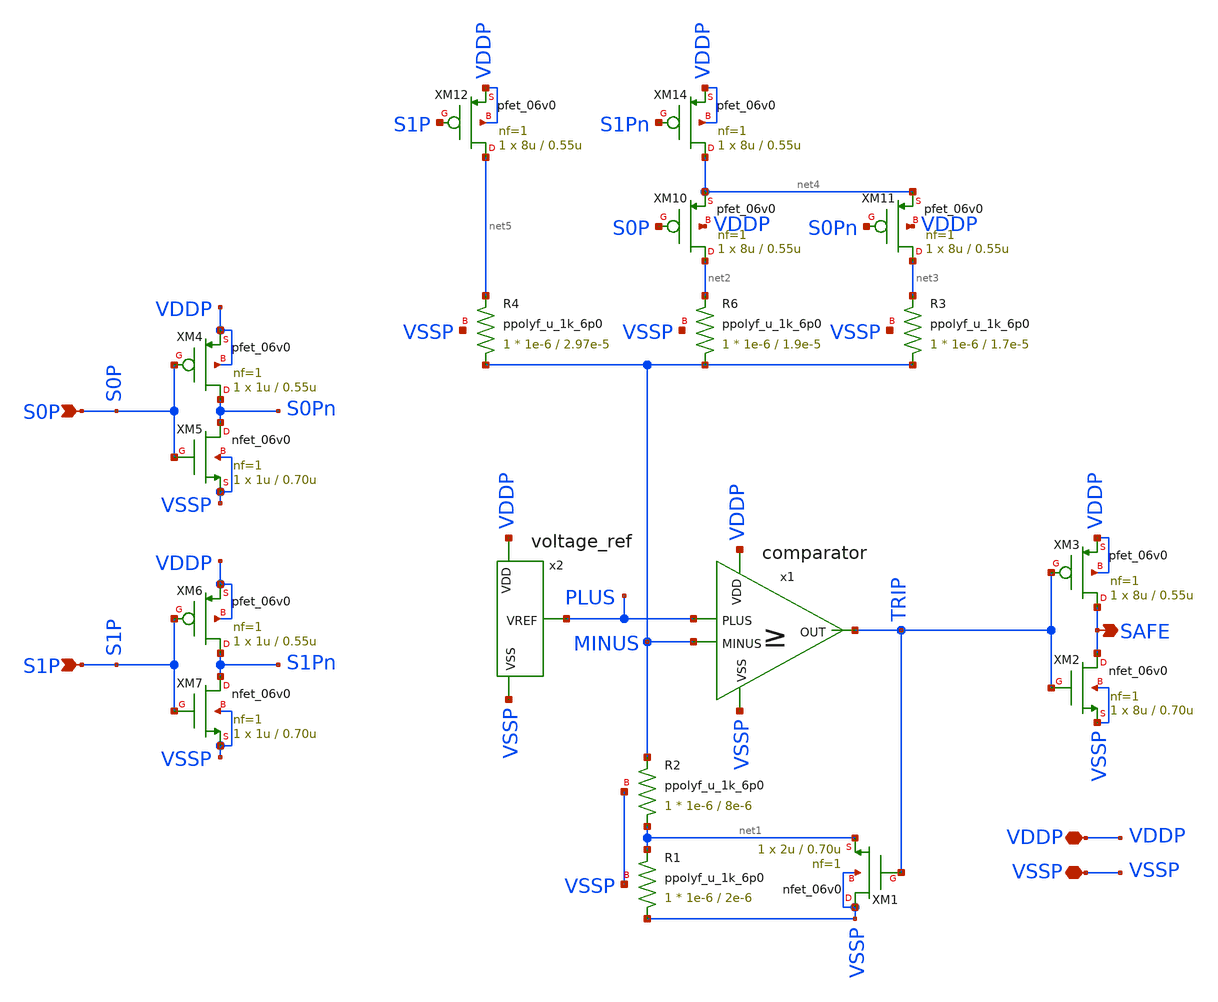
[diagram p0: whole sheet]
** sch_path: analog/xschem/overdischarge_prot.sch
**.subckt overdischarge_prot VDDP VSSP SAFE S0P S1P
*.iopin VDDP
*.iopin VSSP
*.opin SAFE
*.ipin S0P
*.ipin S1P
x1 VDDP TRIP PLUS MINUS VSSP comparator
x2 VDDP PLUS VSSP voltage_ref
XM1 VSSP TRIP net1 VSSP nfet_06v0 L=0.70u W=2u nf=1 ad='int((nf+1)/2) * W/nf * 0.18u' as='int((nf+2)/2) * W/nf * 0.18u'
+ pd='2*int((nf+1)/2) * (W/nf + 0.18u)' ps='2*int((nf+2)/2) * (W/nf + 0.18u)' nrd='0.18u / W' nrs='0.18u / W'
+ sa=0 sb=0 sd=0 m=1
XR1 VSSP net1 VSSP ppolyf_u_1k_6p0 r_width=1e-6 r_length=2e-6 m=1
XR2 net1 MINUS VSSP ppolyf_u_1k_6p0 r_width=1e-6 r_length=8e-6 m=1
XR3 MINUS net3 VSSP ppolyf_u_1k_6p0 r_width=1e-6 r_length=1.7e-5 m=1
XM2 SAFE TRIP VSSP VSSP nfet_06v0 L=0.70u W=8u nf=1 ad='int((nf+1)/2) * W/nf * 0.18u' as='int((nf+2)/2) * W/nf * 0.18u'
+ pd='2*int((nf+1)/2) * (W/nf + 0.18u)' ps='2*int((nf+2)/2) * (W/nf + 0.18u)' nrd='0.18u / W' nrs='0.18u / W'
+ sa=0 sb=0 sd=0 m=1
XM3 SAFE TRIP VDDP VDDP pfet_06v0 L=0.55u W=8u nf=1 ad='int((nf+1)/2) * W/nf * 0.18u' as='int((nf+2)/2) * W/nf * 0.18u'
+ pd='2*int((nf+1)/2) * (W/nf + 0.18u)' ps='2*int((nf+2)/2) * (W/nf + 0.18u)' nrd='0.18u / W' nrs='0.18u / W'
+ sa=0 sb=0 sd=0 m=1
XM4 S0Pn S0P VDDP VDDP pfet_06v0 L=0.55u W=1u nf=1 ad='int((nf+1)/2) * W/nf * 0.18u' as='int((nf+2)/2) * W/nf * 0.18u'
+ pd='2*int((nf+1)/2) * (W/nf + 0.18u)' ps='2*int((nf+2)/2) * (W/nf + 0.18u)' nrd='0.18u / W' nrs='0.18u / W'
+ sa=0 sb=0 sd=0 m=1
XM5 S0Pn S0P VSSP VSSP nfet_06v0 L=0.70u W=1u nf=1 ad='int((nf+1)/2) * W/nf * 0.18u' as='int((nf+2)/2) * W/nf * 0.18u'
+ pd='2*int((nf+1)/2) * (W/nf + 0.18u)' ps='2*int((nf+2)/2) * (W/nf + 0.18u)' nrd='0.18u / W' nrs='0.18u / W'
+ sa=0 sb=0 sd=0 m=1
XM6 S1Pn S1P VDDP VDDP pfet_06v0 L=0.55u W=1u nf=1 ad='int((nf+1)/2) * W/nf * 0.18u' as='int((nf+2)/2) * W/nf * 0.18u'
+ pd='2*int((nf+1)/2) * (W/nf + 0.18u)' ps='2*int((nf+2)/2) * (W/nf + 0.18u)' nrd='0.18u / W' nrs='0.18u / W'
+ sa=0 sb=0 sd=0 m=1
XM7 S1Pn S1P VSSP VSSP nfet_06v0 L=0.70u W=1u nf=1 ad='int((nf+1)/2) * W/nf * 0.18u' as='int((nf+2)/2) * W/nf * 0.18u'
+ pd='2*int((nf+1)/2) * (W/nf + 0.18u)' ps='2*int((nf+2)/2) * (W/nf + 0.18u)' nrd='0.18u / W' nrs='0.18u / W'
+ sa=0 sb=0 sd=0 m=1
XR4 MINUS net5 VSSP ppolyf_u_1k_6p0 r_width=1e-6 r_length=2.97e-5 m=1
XR6 MINUS net2 VSSP ppolyf_u_1k_6p0 r_width=1e-6 r_length=1.9e-5 m=1
XM10 net2 S0P net4 VDDP pfet_06v0 L=0.55u W=8u nf=1 ad='int((nf+1)/2) * W/nf * 0.18u' as='int((nf+2)/2) * W/nf * 0.18u'
+ pd='2*int((nf+1)/2) * (W/nf + 0.18u)' ps='2*int((nf+2)/2) * (W/nf + 0.18u)' nrd='0.18u / W' nrs='0.18u / W'
+ sa=0 sb=0 sd=0 m=1
XM11 net3 S0Pn net4 VDDP pfet_06v0 L=0.55u W=8u nf=1 ad='int((nf+1)/2) * W/nf * 0.18u' as='int((nf+2)/2) * W/nf * 0.18u'
+ pd='2*int((nf+1)/2) * (W/nf + 0.18u)' ps='2*int((nf+2)/2) * (W/nf + 0.18u)' nrd='0.18u / W' nrs='0.18u / W'
+ sa=0 sb=0 sd=0 m=1
XM12 net5 S1P VDDP VDDP pfet_06v0 L=0.55u W=8u nf=1 ad='int((nf+1)/2) * W/nf * 0.18u' as='int((nf+2)/2) * W/nf * 0.18u'
+ pd='2*int((nf+1)/2) * (W/nf + 0.18u)' ps='2*int((nf+2)/2) * (W/nf + 0.18u)' nrd='0.18u / W' nrs='0.18u / W'
+ sa=0 sb=0 sd=0 m=1
XM14 net4 S1Pn VDDP VDDP pfet_06v0 L=0.55u W=8u nf=1 ad='int((nf+1)/2) * W/nf * 0.18u' as='int((nf+2)/2) * W/nf * 0.18u'
+ pd='2*int((nf+1)/2) * (W/nf + 0.18u)' ps='2*int((nf+2)/2) * (W/nf + 0.18u)' nrd='0.18u / W' nrs='0.18u / W'
+ sa=0 sb=0 sd=0 m=1
**.ends

* expanding   symbol:  comparator.sym # of pins=5
** sym_path: analog/xschem/comparator.sym
** sch_path: analog/xschem/comparator.sch
.subckt comparator VDD OUT PLUS MINUS VSS
*.ipin VDD
*.ipin PLUS
*.ipin VSS
*.opin OUT
*.ipin MINUS
XM3 i1 net1 VDD VDD pfet_06v0 L=1.1u W=3u nf=1 ad='int((nf+1)/2) * W/nf * 0.18u' as='int((nf+2)/2) * W/nf * 0.18u'
+ pd='2*int((nf+1)/2) * (W/nf + 0.18u)' ps='2*int((nf+2)/2) * (W/nf + 0.18u)' nrd='0.18u / W' nrs='0.18u / W'
+ sa=0 sb=0 sd=0 m=1
XM4 net2 MINUS VDD VDD pfet_06v0 L=1.1u W=3u nf=1 ad='int((nf+1)/2) * W/nf * 0.18u' as='int((nf+2)/2) * W/nf * 0.18u'
+ pd='2*int((nf+1)/2) * (W/nf + 0.18u)' ps='2*int((nf+2)/2) * (W/nf + 0.18u)' nrd='0.18u / W' nrs='0.18u / W'
+ sa=0 sb=0 sd=0 m=1
XM5 net1 PLUS VDD VDD pfet_06v0 L=1.1u W=3u nf=1 ad='int((nf+1)/2) * W/nf * 0.18u' as='int((nf+2)/2) * W/nf * 0.18u'
+ pd='2*int((nf+1)/2) * (W/nf + 0.18u)' ps='2*int((nf+2)/2) * (W/nf + 0.18u)' nrd='0.18u / W' nrs='0.18u / W'
+ sa=0 sb=0 sd=0 m=1
XM6 net2 net2 VSS VSS nfet_06v0 L=1.4u W=3u nf=1 ad='int((nf+1)/2) * W/nf * 0.18u' as='int((nf+2)/2) * W/nf * 0.18u'
+ pd='2*int((nf+1)/2) * (W/nf + 0.18u)' ps='2*int((nf+2)/2) * (W/nf + 0.18u)' nrd='0.18u / W' nrs='0.18u / W'
+ sa=0 sb=0 sd=0 m=1
XM7 net1 net2 VSS VSS nfet_06v0 L=1.4u W=3u nf=1 ad='int((nf+1)/2) * W/nf * 0.18u' as='int((nf+2)/2) * W/nf * 0.18u'
+ pd='2*int((nf+1)/2) * (W/nf + 0.18u)' ps='2*int((nf+2)/2) * (W/nf + 0.18u)' nrd='0.18u / W' nrs='0.18u / W'
+ sa=0 sb=0 sd=0 m=1
XM8 i1 net1 VSS VSS nfet_06v0 L=1.4u W=3u nf=1 ad='int((nf+1)/2) * W/nf * 0.18u' as='int((nf+2)/2) * W/nf * 0.18u'
+ pd='2*int((nf+1)/2) * (W/nf + 0.18u)' ps='2*int((nf+2)/2) * (W/nf + 0.18u)' nrd='0.18u / W' nrs='0.18u / W'
+ sa=0 sb=0 sd=0 m=1
x1 VDD i1 net3 VSS schmitt
XM9 OUT net3 VDD VDD pfet_06v0 L=0.55u W=24u nf=3 ad='int((nf+1)/2) * W/nf * 0.18u' as='int((nf+2)/2) * W/nf * 0.18u'
+ pd='2*int((nf+1)/2) * (W/nf + 0.18u)' ps='2*int((nf+2)/2) * (W/nf + 0.18u)' nrd='0.18u / W' nrs='0.18u / W'
+ sa=0 sb=0 sd=0 m=1
XM10 OUT net3 VSS VSS nfet_06v0 L=0.70u W=24u nf=3 ad='int((nf+1)/2) * W/nf * 0.18u' as='int((nf+2)/2) * W/nf * 0.18u'
+ pd='2*int((nf+1)/2) * (W/nf + 0.18u)' ps='2*int((nf+2)/2) * (W/nf + 0.18u)' nrd='0.18u / W' nrs='0.18u / W'
+ sa=0 sb=0 sd=0 m=1
.ends


* expanding   symbol:  voltage_ref.sym # of pins=3
** sym_path: analog/xschem/voltage_ref.sym
** sch_path: analog/xschem/voltage_ref.sch
.subckt voltage_ref VDD VREF VSS
*.ipin VDD
*.ipin VSS
*.opin VREF
XM1 net1 net1 VDD VDD pfet_06v0 L=5u W=10u nf=1 ad='int((nf+1)/2) * W/nf * 0.18u' as='int((nf+2)/2) * W/nf * 0.18u'
+ pd='2*int((nf+1)/2) * (W/nf + 0.18u)' ps='2*int((nf+2)/2) * (W/nf + 0.18u)' nrd='0.18u / W' nrs='0.18u / W'
+ sa=0 sb=0 sd=0 m=1
XM2 net2 net1 VDD VDD pfet_06v0 L=5u W=10u nf=1 ad='int((nf+1)/2) * W/nf * 0.18u' as='int((nf+2)/2) * W/nf * 0.18u'
+ pd='2*int((nf+1)/2) * (W/nf + 0.18u)' ps='2*int((nf+2)/2) * (W/nf + 0.18u)' nrd='0.18u / W' nrs='0.18u / W'
+ sa=0 sb=0 sd=0 m=1
XM3 VREF net1 VDD VDD pfet_06v0 L=5u W=10u nf=1 ad='int((nf+1)/2) * W/nf * 0.18u' as='int((nf+2)/2) * W/nf * 0.18u'
+ pd='2*int((nf+1)/2) * (W/nf + 0.18u)' ps='2*int((nf+2)/2) * (W/nf + 0.18u)' nrd='0.18u / W' nrs='0.18u / W'
+ sa=0 sb=0 sd=0 m=1
XM4 net1 net2 net3 VSS nfet_06v0 L=2.5u W=10u nf=1 ad='int((nf+1)/2) * W/nf * 0.18u' as='int((nf+2)/2) * W/nf * 0.18u'
+ pd='2*int((nf+1)/2) * (W/nf + 0.18u)' ps='2*int((nf+2)/2) * (W/nf + 0.18u)' nrd='0.18u / W' nrs='0.18u / W'
+ sa=0 sb=0 sd=0 m=1
XM5 net2 net2 net5 VSS nfet_06v0 L=2.5u W=10u nf=1 ad='int((nf+1)/2) * W/nf * 0.18u' as='int((nf+2)/2) * W/nf * 0.18u'
+ pd='2*int((nf+1)/2) * (W/nf + 0.18u)' ps='2*int((nf+2)/2) * (W/nf + 0.18u)' nrd='0.18u / W' nrs='0.18u / W'
+ sa=0 sb=0 sd=0 m=1
XR1 net4 net3 VSS ppolyf_u_1k_6p0 r_width=1e-6 r_length=5e-6 m=1
XR2 net6 VREF VSS ppolyf_u_1k_6p0 r_width=1e-6 r_length=5e-6 m=1
D3 net6 VSS diode_pd2nw_06v0 area='5u * 1u ' pj='2*5u + 2*1u ' m=1
D1 net5 VSS diode_pd2nw_06v0 area='5u * 1u ' pj='2*5u + 2*1u ' m=1
D2 net4 VSS diode_pd2nw_06v0 area='5u * 1u ' pj='2*5u + 2*1u ' m=1
.ends


* expanding   symbol:  schmitt.sym # of pins=4
** sym_path: analog/xschem/schmitt.sym
** sch_path: analog/xschem/schmitt.sch
.subckt schmitt VDD A Y VSS
*.ipin VDD
*.ipin VSS
*.ipin A
*.opin Y
XM1 net1 A VDD VDD pfet_06v0 L=0.55u W=4u nf=1 ad='int((nf+1)/2) * W/nf * 0.18u' as='int((nf+2)/2) * W/nf * 0.18u'
+ pd='2*int((nf+1)/2) * (W/nf + 0.18u)' ps='2*int((nf+2)/2) * (W/nf + 0.18u)' nrd='0.18u / W' nrs='0.18u / W'
+ sa=0 sb=0 sd=0 m=1
XM2 Y A net1 VDD pfet_06v0 L=0.55u W=4u nf=1 ad='int((nf+1)/2) * W/nf * 0.18u' as='int((nf+2)/2) * W/nf * 0.18u'
+ pd='2*int((nf+1)/2) * (W/nf + 0.18u)' ps='2*int((nf+2)/2) * (W/nf + 0.18u)' nrd='0.18u / W' nrs='0.18u / W'
+ sa=0 sb=0 sd=0 m=1
XM3 Y A net2 VSS nfet_06v0 L=0.70u W=4u nf=1 ad='int((nf+1)/2) * W/nf * 0.18u' as='int((nf+2)/2) * W/nf * 0.18u'
+ pd='2*int((nf+1)/2) * (W/nf + 0.18u)' ps='2*int((nf+2)/2) * (W/nf + 0.18u)' nrd='0.18u / W' nrs='0.18u / W'
+ sa=0 sb=0 sd=0 m=1
XM4 net2 A VSS VSS nfet_06v0 L=0.70u W=4u nf=1 ad='int((nf+1)/2) * W/nf * 0.18u' as='int((nf+2)/2) * W/nf * 0.18u'
+ pd='2*int((nf+1)/2) * (W/nf + 0.18u)' ps='2*int((nf+2)/2) * (W/nf + 0.18u)' nrd='0.18u / W' nrs='0.18u / W'
+ sa=0 sb=0 sd=0 m=1
XM5 VSS Y net1 VDD pfet_06v0 L=0.55u W=2u nf=1 ad='int((nf+1)/2) * W/nf * 0.18u' as='int((nf+2)/2) * W/nf * 0.18u'
+ pd='2*int((nf+1)/2) * (W/nf + 0.18u)' ps='2*int((nf+2)/2) * (W/nf + 0.18u)' nrd='0.18u / W' nrs='0.18u / W'
+ sa=0 sb=0 sd=0 m=1
XM6 VDD Y net2 VSS nfet_06v0 L=0.70u W=2u nf=1 ad='int((nf+1)/2) * W/nf * 0.18u' as='int((nf+2)/2) * W/nf * 0.18u'
+ pd='2*int((nf+1)/2) * (W/nf + 0.18u)' ps='2*int((nf+2)/2) * (W/nf + 0.18u)' nrd='0.18u / W' nrs='0.18u / W'
+ sa=0 sb=0 sd=0 m=1
.ends

.end
